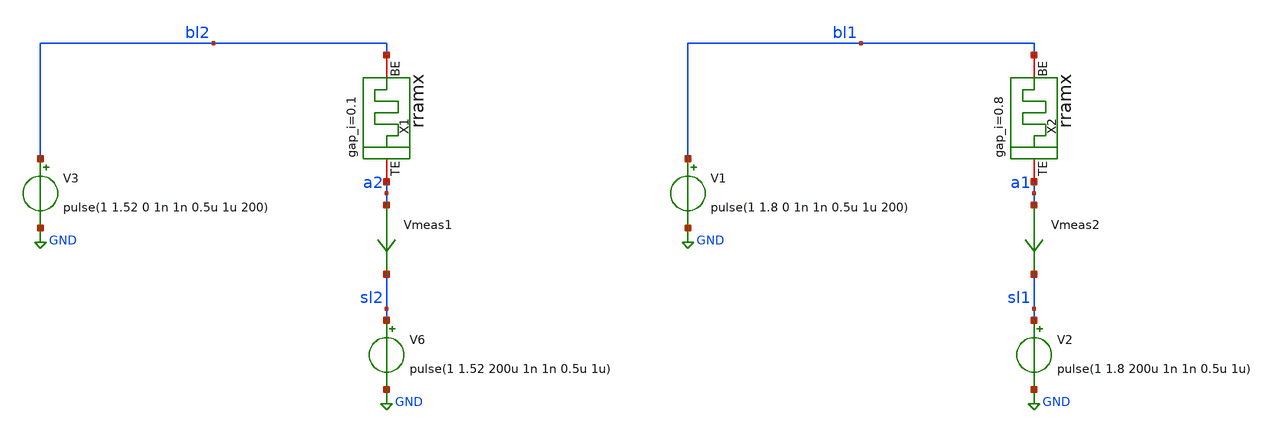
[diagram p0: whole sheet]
** sch_path: designs/tb_memristor/tb_rram_v1_t2.sch
**.subckt tb_rram_v1_t2
V3 bl2 GND pulse(1 1.52 0 1n 1n 0.5u 1u 200)
V6 sl2 GND pulse(1 1.52 200u 1n 1n 0.5u 1u)
Vmeas1 a2 sl2 0
.save i(vmeas1)
X1 a2 bl2 rram_cell gap_i=0.1
V1 bl1 GND pulse(1 1.8 0 1n 1n 0.5u 1u 200)
V2 sl1 GND pulse(1 1.8 200u 1n 1n 0.5u 1u)
Vmeas2 a1 sl1 0
.save i(vmeas2)
X2 a1 bl1 rram_cell gap_i=0.8
**** begin user architecture code
.lib $::SKYWATER_MODELS/sky130.lib.spice tt


*.option savecurrents
.control
 tran 1n 400u uic
 write tb_rram_v1_t2.raw
.endc
.save all


.subckt rram_cell BE TE gap_i=0.1
N1 BE TE rram_model
.model rram_model rram gap_initial={gap_i}
.ends rram_cell

.control
pre_osdi /foss/designs/spike_130/designs/memristors/rram_v1/rram.osdi
.endc

**** end user architecture code
**.ends
.GLOBAL GND
.end
